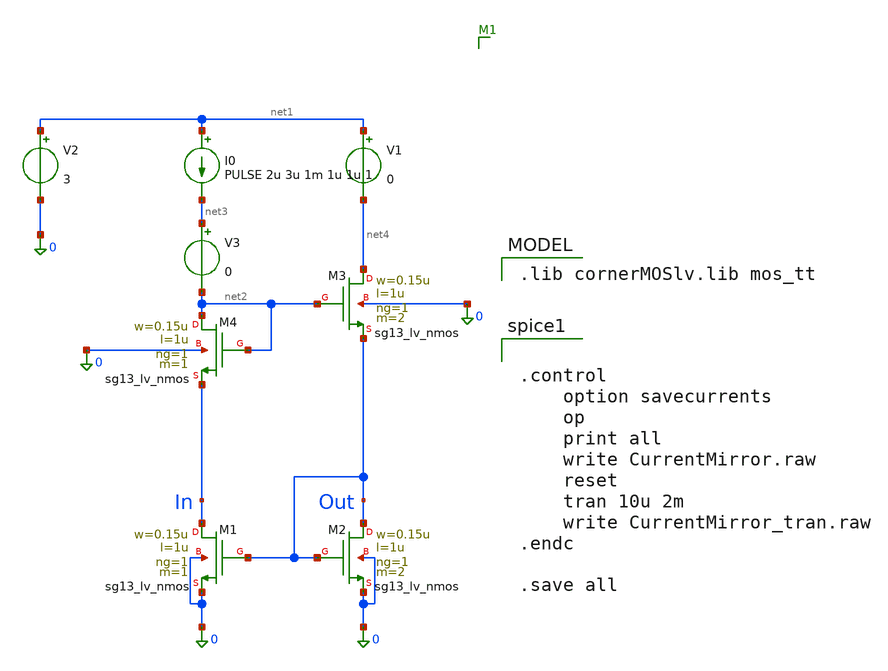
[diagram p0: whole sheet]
** sch_path: src/analog_mac/CurrentMirror.sch
**.subckt CurrentMirror
V1 net1 net4 0
V2 net1 0 3
I0 net1 net3 PULSE 2u 3u 1m 1u 1u 1
XM1 In Out 0 0 sg13_lv_nmos w=0.15u l=1u ng=1 m=1 mm_ok=1
XM2 Out Out 0 0 sg13_lv_nmos w=0.15u l=1u ng=1 m=2 mm_ok=1
V3 net3 net2 0
XM3 net4 net2 Out 0 sg13_lv_nmos w=0.15u l=1u ng=1 m=2 mm_ok=1
XM4 net2 net2 In 0 sg13_lv_nmos w=0.15u l=1u ng=1 m=1 mm_ok=1
**** begin user architecture code
 .lib cornerMOSlv.lib mos_tt



.control
	option savecurrents
	op
	print all
	write CurrentMirror.raw
	reset
	tran 10u 2m
	write CurrentMirror_tran.raw
.endc

.save all


**** end user architecture code
**.ends
.end
